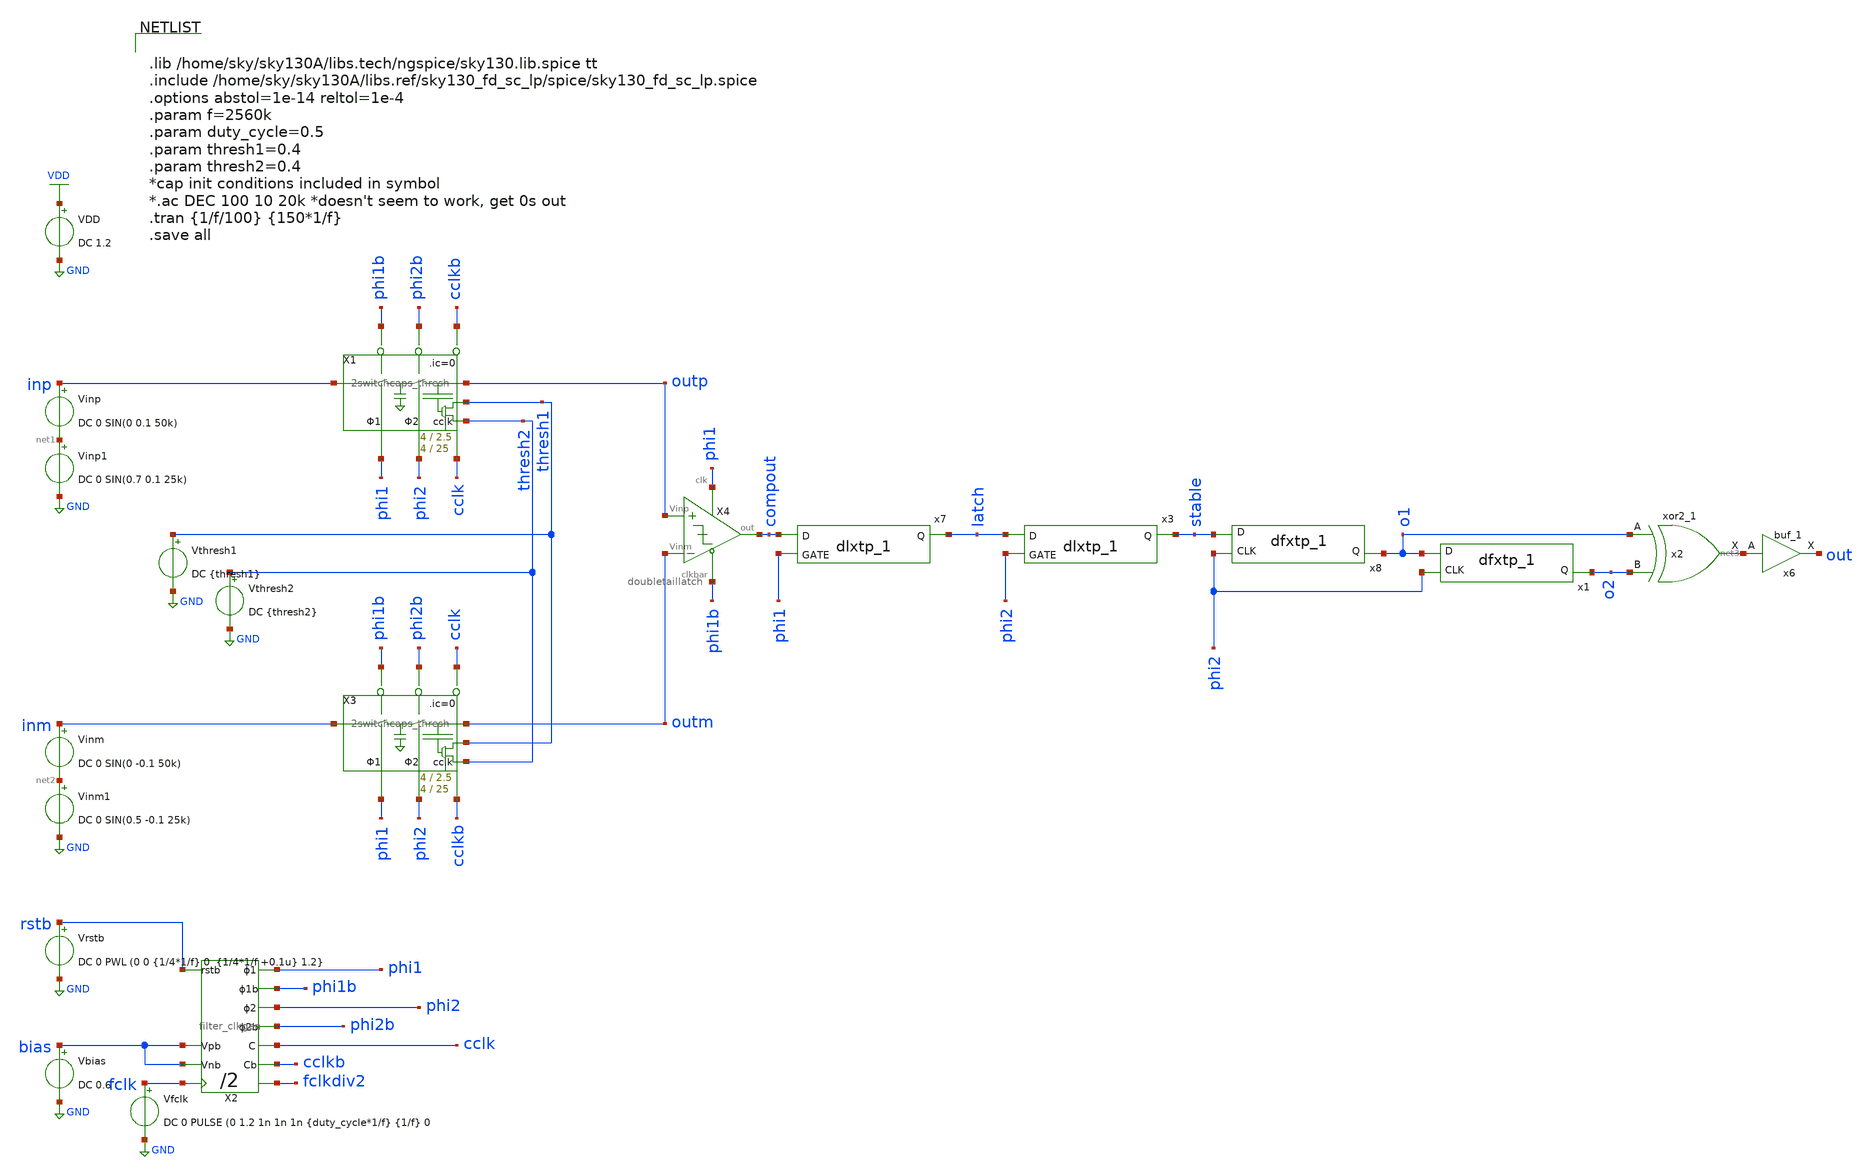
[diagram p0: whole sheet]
** sch_path: xschem/comparator/2switchcaps_thresh_diff_tb.sch
**.subckt 2switchcaps_thresh_diff_tb
Vinp inp net1 DC 0 SIN(0 0.1 50k)
VDD VDD GND DC 1.2
Vfclk fclk GND DC 0 PULSE (0 1.2 1n 1n 1n {duty_cycle*1/f} {1/f} 0
X1 inp outp phi2 phi1 phi1b phi2b thresh2 cclk thresh1 cclkb 2switchcaps_thresh Wcap1=4 Lcap1=2.5
+ Wcap2=4 Lcap2=25
X2 rstb fclk phi2b phi2 phi1b phi1 cclkb cclk fclkdiv2 bias bias filter_clkgen
Vbias bias GND DC 0.6
Vthresh1 thresh1 GND DC {thresh1}
Vthresh2 thresh2 GND DC {thresh2}
Vrstb rstb GND DC 0 PWL (0 0 {1/4*1/f} 0 {1/4*1/f +0.1u} 1.2}
Vinm inm net2 DC 0 SIN(0 -0.1 50k)
X3 inm outm phi2 phi1 phi1b phi2b thresh2 cclkb thresh1 cclk 2switchcaps_thresh Wcap1=4 Lcap1=2.5 Wcap2=4 Lcap2=25
X4 outp outm compout phi1 phi1b doubletaillatch
x2 o1 o2 GND GND VDD VDD net3 sky130_fd_sc_lp__xor2_1
x6 net3 GND GND VDD VDD out sky130_fd_sc_lp__buf_1
x7 compout phi1 gnd gnd vdd vdd latch sky130_fd_sc_lp__dlxtp_1
x8 phi2 stable gnd gnd vdd vdd o1 sky130_fd_sc_lp__dfxtp_1
x1 phi2 o1 gnd gnd vdd vdd o2 sky130_fd_sc_lp__dfxtp_1
Vinp1 net1 GND DC 0 SIN(0.7 0.1 25k)
Vinm1 net2 GND DC 0 SIN(0.5 -0.1 25k)
x3 latch phi2 gnd gnd vdd vdd stable sky130_fd_sc_lp__dlxtp_1
**** begin user architecture code


.lib /home/sky/sky130A/libs.tech/ngspice/sky130.lib.spice tt
.include /home/sky/sky130A/libs.ref/sky130_fd_sc_lp/spice/sky130_fd_sc_lp.spice
.options abstol=1e-14 reltol=1e-4
.param f=2560k
.param duty_cycle=0.5
.param thresh1=0.4
.param thresh2=0.4
*cap init conditions included in symbol
*.ac DEC 100 10 20k *doesn't seem to work, get 0s out
.tran {1/f/100} {150*1/f}
.save all


**** end user architecture code
**.ends
.GLOBAL GND
.GLOBAL VDD
.end
